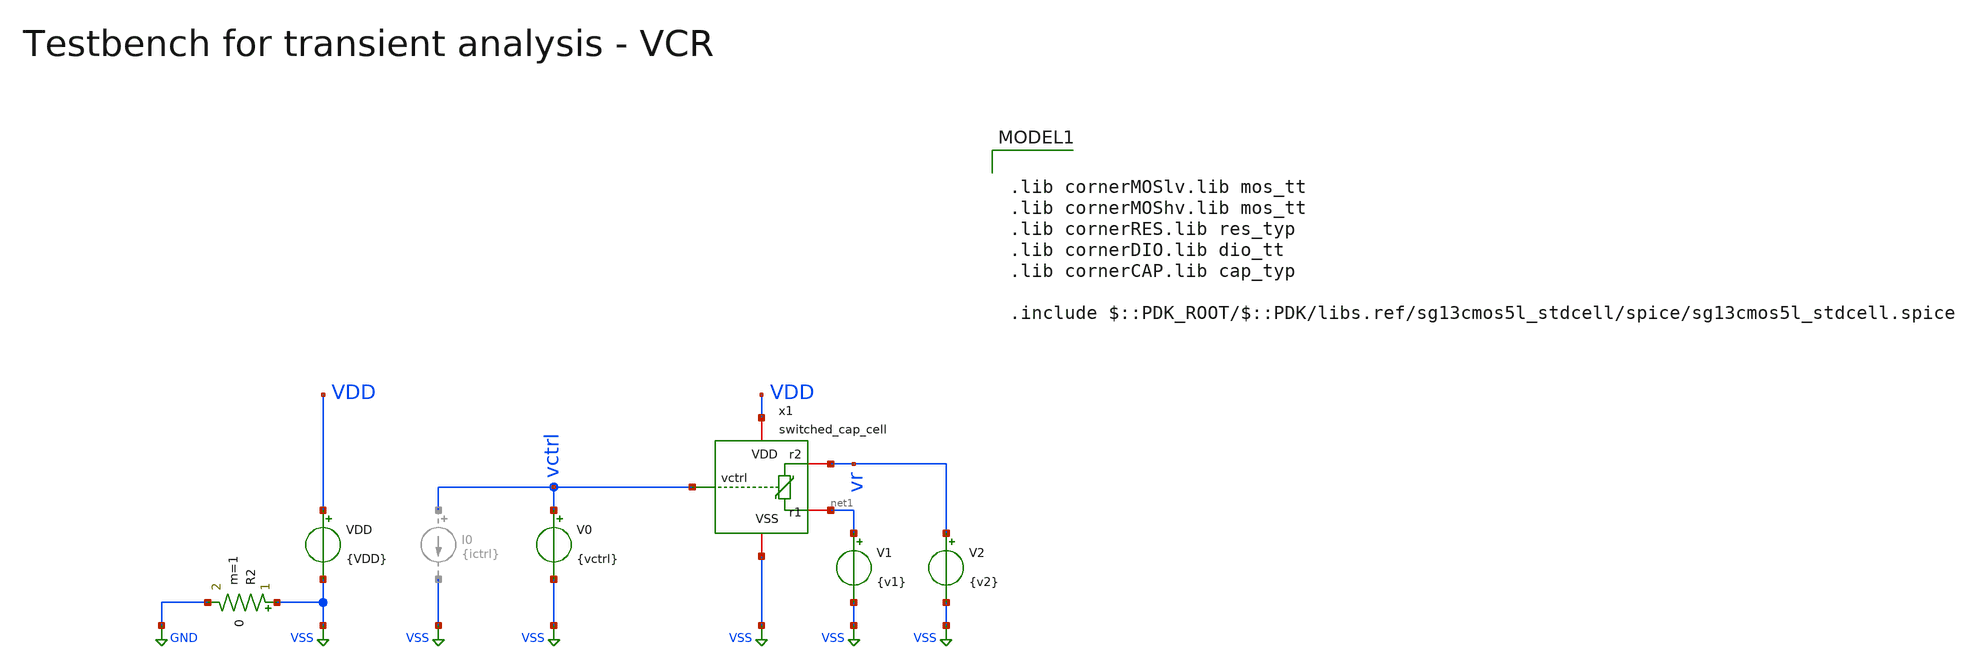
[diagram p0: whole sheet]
** sch_path: macros/heichips26_vcr/macros/switched_capacitor/testbenches/xschem/tb_switched_cap_tran.sch
**.subckt tb_switched_cap_tran
VDD VDD VSS {VDD}
R2 VSS GND 0 m=1
x1 vctrl VDD VSS vr net1 switched_cap_cell
V1 net1 VSS {v1}
V2 vr VSS {v2}
V0 vctrl VSS {vctrl}
**** begin user architecture code

.lib cornerMOSlv.lib mos_tt
.lib cornerMOShv.lib mos_tt
.lib cornerRES.lib res_typ
.lib cornerDIO.lib dio_tt
.lib cornerCAP.lib cap_typ

.include $::PDK_ROOT/$::PDK/libs.ref/sg13cmos5l_stdcell/spice/sg13cmos5l_stdcell.spice



.param temp=27
.param vctrl  = 3.3
.param f      = {2e6/vctrl}

* Derived timing parameters
.param period = {1/f}
.param ton    = {period/2}
.csparam tstop  = {5*period}
.csparam tstep  = {period/100}
.param ictrl  = {f*3.3e-12}
.param tr     = {period/1000}
.param tf     = {period/1000}

.param VDD = 3.3
.csparam VDD=VDD
.param vdm = 3.3
.param vcm = {VDD/2}
.param v1  = {vcm - vdm/2}
.param v2  = {vcm + vdm/2}

.options savecurrents klu method=gear reltol=1e-6 abstol=1e-12 gmin=1e-15
.probe alli
.control

save all
set appendwrite

tran {$&tstep} {$&tstop}
remzerovec

save all
set appendwrite

write @schname\.raw
set appendwrite

*let r_var = vr/i(r1)
meas tran period_sim TRIG i(V1) VAL=1m RISE=1 TARG i(V1) VAL=1m RISE=2
meas tran n_periods TRIG i(V1) VAL=1m RISE=1 TARG i(V1) VAL=1m RISE=LAST
meas tran i_avg AVG i(V1) FROM=0 TO=n_periods
meas tran v_avg AVG vr FROM=0 TO=n_periods
*meas tran r_avg AVG r_var

let npts = length(time) - 1
let i_mavg = integ(i(V1))[1, npts] / time[1, npts]
let v_mavg = integ(vr)[1, npts] / time[1, npts]
let r_mavg = v_mavg/i_mavg
let r_avg = v_avg/i_avg
let f_sim = 1/period_sim
let plot_y_lim = 1.2*r_avg

print period_sim f_sim r_avg

* Plotting
plot vr v_avg v_mavg
plot i(V1) i_avg i_mavg
plot r_avg r_mavg ylimit 0 $&plot_y_lim
plot x1.clk

* Write Data
unset appendwrite
set wr_vecnames
set wr_singlescale
wrdata ../plot_simulations/data/@schname\.txt v(vr) v(VDD) i(V1)

*quit
.endc


**** end user architecture code
**.ends

* expanding   symbol:  switched_cap_cell.sym # of pins=5
** sym_path: macros/heichips26_vcr/macros/switched_capacitor/schematic/xschem/switched_cap_cell.sym
** sch_path: macros/heichips26_vcr/macros/switched_capacitor/schematic/xschem/switched_cap_cell.sch
.subckt switched_cap_cell vctrl VDD VSS r2 r1
*.iopin r1
*.iopin r2
*.iopin VDD
*.iopin VSS
*.iopin vctrl
XC1 net1 VSS cap_cmomi w=30e-6 l=30e-6 mmin=1 mmax=4 feed=double subblock=0 m=1 mm_ok=1
x2 net2 net1 r1 net3 VDD VSS transmission_gate
x6 net5 net1 r2 net4 VDD VSS transmission_gate
x3 net2 net3 VDD clk VSS net5 net4 pulse_shaper
x4 net7 VDD clk VSS VSS VSS VSS net6 net8 hv_mux4
x5 VDD net6 vctrl VSS net9 vco
vselA net7 VSS 0
vselB net8 VSS 3.3
.ends


* expanding   symbol:  transmission_gate.sym # of pins=6
** sym_path: macros/heichips26_vcr/macros/switched_capacitor/schematic/xschem/transmission_gate.sym
** sch_path: macros/heichips26_vcr/macros/switched_capacitor/schematic/xschem/transmission_gate.sch
.subckt transmission_gate vctrl vin vout nvctrl VDD VSS
*.iopin vin
*.iopin vout
*.ipin vctrl
*.ipin nvctrl
*.iopin VDD
*.iopin VSS
XM3 vout vctrl vin VSS sg13_hv_nmos w={tg_ngate_w*tg_ng} l={tg_ch_len} ng={tg_ng} m=1 mm_ok=1
XM4 vout nvctrl vin VDD sg13_hv_pmos w={tg_pgate_w*tg_ng} l={tg_ch_len} ng={tg_ng} m=1 mm_ok=1
**** begin user architecture code


.param tg_ch_len=1u
.param tg_ngate_w=2u
.param tg_pgate_w=10u
.param tg_ng=20


**** end user architecture code
.ends


* expanding   symbol:  osc.sym # of pins=6
** sym_path: macros/heichips26_vcr/macros/switched_capacitor/schematic/xschem/osc.sym
** sch_path: macros/heichips26_vcr/macros/switched_capacitor/schematic/xschem/osc.sch
.subckt osc VDD out1 ictrl VSS start out2
*.iopin VSS
*.iopin VDD
*.iopin out2
*.iopin out1
*.iopin start
*.iopin ictrl
XM3 out1 ictrl VDD VDD sg13_hv_pmos w=10.0u l=2.0u ng=1 m=1 mm_ok=1
XM2 net1 ictrl VDD VDD sg13_hv_pmos w=1u l=2.0u ng=1 m=1 mm_ok=1
XM4 start ictrl VDD VDD sg13_hv_pmos w=1.0u l=2.0u ng=1 m=1 mm_ok=1
XM5 out2 ictrl VDD VDD sg13_hv_pmos w=10.0u l=2.0u ng=1 m=1 mm_ok=1
XM6 ictrl ictrl VDD VDD sg13_hv_pmos w=10.0u l=2.0u ng=1 m=1 mm_ok=1
XC1 net1 out1 cap_cmomi w=10e-6 l=10e-6 mmin=1 mmax=4 feed=double subblock=0 m=1 mm_ok=1
XC2 out2 start cap_cmomi w=10e-6 l=10e-6 mmin=1 mmax=4 feed=double subblock=0 m=1 mm_ok=1
XM8 out1 start VSS VSS sg13_hv_nmos w=3u l=0.45u ng=1 m=1 mm_ok=1
XM1 start start VSS VSS sg13_hv_nmos w=1u l=2u ng=1 m=1 mm_ok=1
XM12 out2 net1 VSS VSS sg13_hv_nmos w=3u l=0.45u ng=1 m=1 mm_ok=1
XM11 net1 net1 VSS VSS sg13_hv_nmos w=1u l=2u ng=1 m=1 mm_ok=1
**** begin user architecture code


.ic v(out1)=0 v(out2)=3.3


**** end user architecture code
.ends


* expanding   symbol:  pulse_shaper.sym # of pins=7
** sym_path: macros/heichips26_vcr/macros/switched_capacitor/schematic/xschem/pulse_shaper.sym
** sch_path: macros/heichips26_vcr/macros/switched_capacitor/schematic/xschem/pulse_shaper.sch
.subckt pulse_shaper out1 nout1 VDD in VSS out2 nout2
*.opin out1
*.opin nout1
*.opin out2
*.opin nout2
*.ipin in
*.iopin VSS
*.iopin VDD
x4 VDD net3 nout2 VSS hv_inverter_40u
x7 VDD net1 net3 VSS low_th_inverter
x8 VDD net1 net2 VSS high_th_inverter
x9 VDD net2 out1 VSS hv_inverter_40u
x10 VDD out1 nout1 VSS hv_inverter_40u
x11 VDD nout2 out2 VSS hv_inverter_40u
**** begin user architecture code


.include ../../../netlist/pex/hv_inverter_0u3_magic_pex_3.spice
.param w   = 0.3u
.param ng  = 1
.param n_ng = ng
.param n_w = {w*n_ng}
.param n_l = 0.45u
.param p_ng = ng
.param p_w = {1*w*p_ng}
.param p_l = 0.4u


**** end user architecture code
x1 VDD in net1 VSS hv_inverter_0u3
.ends


* expanding   symbol:  hv_mux4.sym # of pins=9
** sym_path: macros/heichips26_vcr/macros/switched_capacitor/schematic/xschem/hv_mux4.sym
** sch_path: macros/heichips26_vcr/macros/switched_capacitor/schematic/xschem/hv_mux4.sch
.subckt hv_mux4 selA VDD out VSS in3 in1 in4 in2 selB
*.ipin in1
*.iopin VDD
*.iopin VSS
*.opin out
*.ipin in2
*.ipin selA
*.ipin in3
*.ipin in4
*.ipin selB
x3 VDD selA net9 VSS hv_inverter_40u
x1 VDD net2 out net1 VSS net3 net4 hv_nor4
x2 VDD in1 net2 net6 VSS hv_nor
x4 VDD in2 net1 net7 VSS hv_nor
x5 VDD in3 net3 net8 VSS hv_nor
x6 VDD in4 net4 net5 VSS hv_nor
x7 VDD selA net5 selB VSS hv_nand
x9 VDD net9 net7 selB VSS hv_nand
x10 VDD selB net10 VSS hv_inverter_40u
x11 VDD selA net8 net10 VSS hv_nand
x8 VDD net9 net6 net10 VSS hv_nand
.ends


* expanding   symbol:  vco.sym # of pins=5
** sym_path: macros/heichips26_vcr/macros/switched_capacitor/schematic/xschem/vco.sym
** sch_path: macros/heichips26_vcr/macros/switched_capacitor/schematic/xschem/vco.sch
.subckt vco VDD out vctrl VSS nout
*.iopin VSS
*.iopin VDD
*.iopin nout
*.iopin out
*.iopin vctrl
**** begin user architecture code


.ic v(vc)=1.65


**** end user architecture code
XC1 vc VSS cap_cmomi w=30e-6 l=30e-6 mmin=1 mmax=4 feed=double subblock=0 m=1 mm_ok=1
XM4 vc out 5uA- VSS sg13_hv_nmos w=0.3u l=0.45u ng=1 m=1 mm_ok=1
x1 VDD s out nout r VSS hv_rs-ff
**** begin user architecture code


.param cm_n_w = 6u
.param cm_n_l = 5u
.param cm_p_w = 10u
.param cm_p_l = 2u

.param inv_ng = 1
.param inv_n_w = 2u
.param inv_n_l = 0.45u
.param inv_p_w = 6.5u
.param inv_p_l = 0.4u


**** end user architecture code
XM6 vc out 5uA+ VDD sg13_hv_pmos w=0.3u l=0.4u ng=1 m=1 mm_ok=1
x5 net2 vc vthl VDD 40uA- VSS comp_pmos
x4 VDD net3 VSS current_reference_40uA
XM7 s net1 VSS VSS sg13_hv_nmos w=inv_n_w l=inv_n_l ng=inv_ng m=1 mm_ok=1
XM8 s net1 VDD VDD sg13_hv_pmos w=inv_p_w l=inv_p_l ng=inv_ng m=1 mm_ok=1
XM9 r net2 VSS VSS sg13_hv_nmos w=inv_n_w l=inv_n_l ng=inv_ng m=1 mm_ok=1
XM10 r net2 VDD VDD sg13_hv_pmos w=inv_p_w l=inv_p_l ng=inv_ng m=1 mm_ok=1
x7 net1 vthh vc VDD 40uA+ VSS comp_nmos
XM11 net3 net3 VDD VDD sg13_hv_pmos w=cm_p_w l=cm_p_l ng=1 m=1 mm_ok=1
XM12 40uA+ net3 VDD VDD sg13_hv_pmos w=cm_p_w l=cm_p_l ng=1 m=1 mm_ok=1
XM13 net4 net3 VDD VDD sg13_hv_pmos w=cm_p_w l=cm_p_l ng=1 m=1 mm_ok=1
XM14 net4 net4 VSS VSS sg13_hv_nmos w=cm_n_w l=cm_n_l ng=1 m=1 mm_ok=1
XM15 40uA- net4 VSS VSS sg13_hv_nmos w=cm_n_w l=cm_n_l ng=1 m=1 mm_ok=1
x2 10uA- vthl VDD vctrl VSS vthh voltage_mirror_pmos
XM1 net5 net3 VDD VDD sg13_hv_pmos w=cm_p_w l=cm_p_l ng=1 m=1 mm_ok=1
XM2 net5 net5 VSS VSS sg13_hv_nmos w=4*cm_n_w l=cm_n_l ng=4 m=1 mm_ok=1
XM3 10uA- net5 VSS VSS sg13_hv_nmos w=cm_n_w l=cm_n_l ng=1 m=1 mm_ok=1
XM5 net6 net5 VSS VSS sg13_hv_nmos w=cm_n_w l=cm_n_l ng=1 m=1 mm_ok=1
XM25 net6 net6 VDD VDD sg13_hv_pmos w=2*cm_p_w l=cm_p_l ng=2 m=1 mm_ok=1
XM26 net7 net6 VDD VDD sg13_hv_pmos w=cm_p_w l=cm_p_l ng=1 m=1 mm_ok=1
XM27 5uA+ net6 VDD VDD sg13_hv_pmos w=cm_p_w l=cm_p_l ng=1 m=1 mm_ok=1
XM28 net7 net7 VSS VSS sg13_hv_nmos w=2*cm_n_w l=cm_n_l ng=2 m=1 mm_ok=1
XM29 5uA- net7 VSS VSS sg13_hv_nmos w=cm_n_w l=cm_n_l ng=1 m=1 mm_ok=1
.ends


* expanding   symbol:  hv_inverter_40u.sym # of pins=4
** sym_path: macros/heichips26_vcr/macros/switched_capacitor/schematic/xschem/hv_inverter_40u.sym
** sch_path: macros/heichips26_vcr/macros/switched_capacitor/schematic/xschem/hv_inverter_40u.sch
.subckt hv_inverter_40u VDD in out VSS
*.ipin in
*.iopin VDD
*.iopin VSS
*.opin out
XM2 out in VSS VSS sg13_hv_nmos w={n_w} l={n_l} ng={ng} m=1 mm_ok=1
XM3 out in VDD VDD sg13_hv_pmos w={p_w} l={p_l} ng={ng} m=1 mm_ok=1
**** begin user architecture code


.param w   = 10u
.param ng  = 4
.param n_ng = ng
.param n_w = {3u*n_ng}
.param n_l = 0.45u
.param p_ng = ng
.param p_w = {10u*p_ng}
.param p_l = 0.4u


**** end user architecture code
.ends


* expanding   symbol:  low_th_inverter.sym # of pins=4
** sym_path: macros/heichips26_vcr/macros/switched_capacitor/schematic/xschem/low_th_inverter.sym
** sch_path: macros/heichips26_vcr/macros/switched_capacitor/schematic/xschem/low_th_inverter.sch
.subckt low_th_inverter VDD vin vout VSS
*.ipin vin
*.iopin VDD
*.iopin VSS
*.opin vout
XM1 vout vin VSS VSS sg13_hv_nmos w={n_ng*n_w} l={n_l} ng={n_ng} m=1 mm_ok=1
XM2 vout vin VDD VDD sg13_hv_pmos w={p_ng*p_w} l={p_l} ng={n_ng} m=1 mm_ok=1
**** begin user architecture code


.param n_ng = 2
.param n_w = 1u
.param n_l = 0.45u
.param p_ng = 2
.param p_w = 1u
.param p_l = 0.4u


**** end user architecture code
.ends


* expanding   symbol:  high_th_inverter.sym # of pins=4
** sym_path: macros/heichips26_vcr/macros/switched_capacitor/schematic/xschem/high_th_inverter.sym
** sch_path: macros/heichips26_vcr/macros/switched_capacitor/schematic/xschem/high_th_inverter.sch
.subckt high_th_inverter VDD vin vout VSS
*.ipin vin
*.iopin VDD
*.iopin VSS
*.opin vout
XMdummy1 VSS VSS VSS VSS sg13_hv_nmos w=0.6u l=1.0u ng=2 m=1 mm_ok=1
XMdummy2 VDD VDD VDD VDD sg13_hv_pmos w=12.0u l=1.0u ng=2 m=1 mm_ok=1
XM1 vout vin VSS VSS sg13_hv_nmos w=6.0u l=1.0u ng=20 m=1 mm_ok=1
XM2 vout vin VDD VDD sg13_hv_pmos w=120.0u l=1.0u ng=20 m=1 mm_ok=1
.ends


* expanding   symbol:  hv_inverter_0u3.sym # of pins=4
** sym_path: macros/heichips26_vcr/macros/switched_capacitor/schematic/xschem/hv_inverter_0u3.sym
** sch_path: macros/heichips26_vcr/macros/switched_capacitor/schematic/xschem/hv_inverter_0u3.sch
.subckt hv_inverter_0u3 VDD in out VSS
*.ipin in
*.iopin VDD
*.iopin VSS
*.opin out
XM2 out in VSS VSS sg13_hv_nmos w={n_w} l={n_l} ng={ng} m=1 mm_ok=1
XM3 out in VDD VDD sg13_hv_pmos w={p_w} l={p_l} ng={ng} m=1 mm_ok=1
**** begin user architecture code


.param w   = 0.3u
.param ng  = 1
.param n_ng = ng
.param n_w = {w*n_ng}
.param n_l = 0.45u
.param p_ng = ng
.param p_w = {1*w*p_ng}
.param p_l = 0.4u


**** end user architecture code
.ends


* expanding   symbol:  hv_nor4.sym # of pins=7
** sym_path: macros/heichips26_vcr/macros/switched_capacitor/schematic/xschem/hv_nor4.sym
** sch_path: macros/heichips26_vcr/macros/switched_capacitor/schematic/xschem/hv_nor4.sch
.subckt hv_nor4 VDD in1 out in2 VSS in3 in4
*.ipin in1
*.iopin VDD
*.iopin VSS
*.opin out
*.ipin in2
*.ipin in3
*.ipin in4
**** begin user architecture code


.param w   = 10u
.param ng  = 4
.param n_ng = ng
.param n_w = {3u*n_ng}
.param n_l = 0.45u
.param p_ng = ng
.param p_w = {10u*p_ng}
.param p_l = 0.4u


**** end user architecture code
XM2 out in3 VSS VSS sg13_hv_nmos w={n_w} l={n_l} ng={ng} m=1 mm_ok=1
XM3 net3 in4 VDD VDD sg13_hv_pmos w={p_w} l={p_l} ng={ng} m=1 mm_ok=1
XM1 out in4 VSS VSS sg13_hv_nmos w={n_w} l={n_l} ng={ng} m=1 mm_ok=1
XM4 out in1 net1 VDD sg13_hv_pmos w={p_w} l={p_l} ng={ng} m=1 mm_ok=1
XM5 out in2 VSS VSS sg13_hv_nmos w={n_w} l={n_l} ng={ng} m=1 mm_ok=1
XM6 out in1 VSS VSS sg13_hv_nmos w={n_w} l={n_l} ng={ng} m=1 mm_ok=1
XM7 net1 in2 net2 VDD sg13_hv_pmos w={p_w} l={p_l} ng={ng} m=1 mm_ok=1
XM8 net2 in3 net3 VDD sg13_hv_pmos w={p_w} l={p_l} ng={ng} m=1 mm_ok=1
.ends


* expanding   symbol:  hv_nor.sym # of pins=5
** sym_path: macros/heichips26_vcr/macros/switched_capacitor/schematic/xschem/hv_nor.sym
** sch_path: macros/heichips26_vcr/macros/switched_capacitor/schematic/xschem/hv_nor.sch
.subckt hv_nor VDD in1 out in2 VSS
*.ipin in1
*.iopin VDD
*.iopin VSS
*.opin out
*.ipin in2
**** begin user architecture code


.param w   = 10u
.param ng  = 4
.param n_ng = ng
.param n_w = {3u*n_ng}
.param n_l = 0.45u
.param p_ng = ng
.param p_w = {10u*p_ng}
.param p_l = 0.4u


**** end user architecture code
XM2 out in1 VSS VSS sg13_hv_nmos w={n_w} l={n_l} ng={ng} m=1 mm_ok=1
XM3 net1 in2 VDD VDD sg13_hv_pmos w={p_w} l={p_l} ng={ng} m=1 mm_ok=1
XM1 out in2 VSS VSS sg13_hv_nmos w={n_w} l={n_l} ng={ng} m=1 mm_ok=1
XM4 out in1 net1 VDD sg13_hv_pmos w={p_w} l={p_l} ng={ng} m=1 mm_ok=1
.ends


* expanding   symbol:  hv_nand.sym # of pins=5
** sym_path: macros/heichips26_vcr/macros/switched_capacitor/schematic/xschem/hv_nand.sym
** sch_path: macros/heichips26_vcr/macros/switched_capacitor/schematic/xschem/hv_nand.sch
.subckt hv_nand VDD in1 out in2 VSS
*.ipin in1
*.iopin VDD
*.iopin VSS
*.opin out
*.ipin in2
**** begin user architecture code


.param w   = 10u
.param ng  = 4
.param n_ng = ng
.param n_w = {3u*n_ng}
.param n_l = 0.45u
.param p_ng = ng
.param p_w = {10u*p_ng}
.param p_l = 0.4u


**** end user architecture code
XM2 out in1 net1 VSS sg13_hv_nmos w={n_w} l={n_l} ng={ng} m=1 mm_ok=1
XM3 out in2 VDD VDD sg13_hv_pmos w={p_w} l={p_l} ng={ng} m=1 mm_ok=1
XM1 net1 in2 VSS VSS sg13_hv_nmos w={n_w} l={n_l} ng={ng} m=1 mm_ok=1
XM4 out in1 VDD VDD sg13_hv_pmos w={p_w} l={p_l} ng={ng} m=1 mm_ok=1
.ends


* expanding   symbol:  hv_rs-ff.sym # of pins=6
** sym_path: macros/heichips26_vcr/macros/switched_capacitor/schematic/xschem/hv_rs-ff.sym
** sch_path: macros/heichips26_vcr/macros/switched_capacitor/schematic/xschem/hv_rs-ff.sch
.subckt hv_rs-ff VDD nS Q nQ nR VSS
*.ipin nS
*.iopin VDD
*.iopin VSS
*.opin Q
*.ipin nR
*.opin nQ
x4 VDD nS Q nQ VSS hv_nand
x5 VDD Q nQ nR VSS hv_nand
.ends


* expanding   symbol:  comp_pmos.sym # of pins=6
** sym_path: macros/heichips26_vcr/macros/switched_capacitor/schematic/xschem/comp_pmos.sym
** sch_path: macros/heichips26_vcr/macros/switched_capacitor/schematic/xschem/comp_pmos.sch
.subckt comp_pmos out - + VDD Ibias VSS
*.iopin VDD
*.iopin VSS
*.ipin Ibias
*.opin out
*.ipin +
*.ipin -
**** begin user architecture code


.param n_w = 1.2u
.param n_l = 1.5u
.param p_w = 2u
.param p_l = 0.4u
.param bcm = 1


**** end user architecture code
XM9 net1 Ibias VDD VDD sg13_hv_pmos w=bcm*p_w l=p_l ng=1 m=1 mm_ok=1
XM10 out Ibias VDD VDD sg13_hv_pmos w=bcm*p_w l=p_l ng=1 m=1 mm_ok=1
XM11 Ibias Ibias VDD VDD sg13_hv_pmos w=p_w l=p_l ng=1 m=1 mm_ok=1
XM12 net3 + net1 VDD sg13_hv_pmos w=p_w l=p_l ng=1 m=1 mm_ok=1
XM13 net2 - net1 VDD sg13_hv_pmos w=p_w l=p_l ng=1 m=1 mm_ok=1
XM14 net3 net2 VSS VSS sg13_hv_nmos w=n_w l=n_l ng=1 m=1 mm_ok=1
XM15 net2 net2 VSS VSS sg13_hv_nmos w=n_w l=n_l ng=1 m=1 mm_ok=1
XM16 out net3 VSS VSS sg13_hv_nmos w=n_w l=n_l ng=1 m=1 mm_ok=1
.ends


* expanding   symbol:  current_reference_40uA.sym # of pins=3
** sym_path: macros/heichips26_vcr/macros/switched_capacitor/schematic/xschem/current_reference_40uA.sym
** sch_path: macros/heichips26_vcr/macros/switched_capacitor/schematic/xschem/current_reference_40uA.sch
.subckt current_reference_40uA VDD iout VSS
*.iopin VSS
*.iopin VDD
*.iopin iout
XM8 net2 net2 VSS VSS sg13_hv_nmos w=n_w l=n_l ng=1 m=1 mm_ok=1
XM6 net2 net1 VDD VDD sg13_hv_pmos w=p_w l=p_l ng=1 m=1 mm_ok=1
XM1 net1 net1 VDD VDD sg13_hv_pmos w=p_w l=p_l ng=1 m=1 mm_ok=1
XM3 net1 net2 net3 VSS sg13_hv_nmos w=n_w l=n_l ng=1 m=1 mm_ok=1
XR2 net4 VSS VSS rppd w=2e-6 l=21.9e-6 m=1 b=0 mm_ok=1
XM2 net1 net2 net3 VSS sg13_hv_nmos w=n_w l=n_l ng=1 m=1 mm_ok=1
XM4 net1 net2 net3 VSS sg13_hv_nmos w=n_w l=n_l ng=1 m=1 mm_ok=1
XM5 net1 net2 net3 VSS sg13_hv_nmos w=n_w l=n_l ng=1 m=1 mm_ok=1
XM7 iout net2 VSS VSS sg13_hv_nmos w=n_w l=n_l ng=1 m=1 mm_ok=1
XR3 net3 net4 VSS rsil w=0.5e-6 l=365e-6 m=1 mm_ok=1
**** begin user architecture code


.param n_w = 6u
.param n_l = 5u
.param p_w = 10u
.param p_l = 2u


**** end user architecture code
.ends


* expanding   symbol:  comp_nmos.sym # of pins=6
** sym_path: macros/heichips26_vcr/macros/switched_capacitor/schematic/xschem/comp_nmos.sym
** sch_path: macros/heichips26_vcr/macros/switched_capacitor/schematic/xschem/comp_nmos.sch
.subckt comp_nmos out - + VDD Ibias VSS
*.iopin VDD
*.iopin VSS
*.ipin -
*.ipin +
*.ipin Ibias
*.opin out
XM8 net2 + net3 VSS sg13_hv_nmos w=n_w l=n_l ng=1 m=1 mm_ok=1
XM6 net1 net1 VDD VDD sg13_hv_pmos w=p_w l=p_l ng=1 m=1 mm_ok=1
XM1 net2 net1 VDD VDD sg13_hv_pmos w=p_w l=p_l ng=1 m=1 mm_ok=1
XM3 net1 - net3 VSS sg13_hv_nmos w=n_w l=n_l ng=1 m=1 mm_ok=1
**** begin user architecture code


.param n_w = 1.2u
.param n_l = 1.5u
.param p_w = 2u
.param p_l = 0.4u


**** end user architecture code
XM2 out net2 VDD VDD sg13_hv_pmos w=p_w l=p_l ng=1 m=1 mm_ok=1
XM4 net3 Ibias VSS VSS sg13_hv_nmos w=2*n_w l=n_l ng=1 m=1 mm_ok=1
XM5 out Ibias VSS VSS sg13_hv_nmos w=2*n_w l=n_l ng=1 m=1 mm_ok=1
XM7 Ibias Ibias VSS VSS sg13_hv_nmos w=n_w l=n_l ng=1 m=1 mm_ok=1
.ends


* expanding   symbol:  voltage_mirror_pmos.sym # of pins=6
** sym_path: macros/heichips26_vcr/macros/switched_capacitor/schematic/xschem/voltage_mirror_pmos.sym
** sch_path: macros/heichips26_vcr/macros/switched_capacitor/schematic/xschem/voltage_mirror_pmos.sch
.subckt voltage_mirror_pmos Ibias nout VDD in VSS out
*.iopin VDD
*.iopin VSS
*.ipin in
*.opin out
*.opin nout
*.ipin Ibias
**** begin user architecture code


.param n_w = 6u
.param n_l = 5u
.param p_w = 10u
.param p_l = 2u


**** end user architecture code
XR1 in Ibias VSS rhigh w=0.5e-6 l=34e-6 m=1 b=0 mm_ok=1
XM4 net1 Ibias VDD VDD sg13_hv_pmos w=p_w l=p_l ng=1 m=1 mm_ok=1
XM5 out net1 VSS VSS sg13_hv_nmos w=n_w l=n_l ng=1 m=1 mm_ok=1
XR2 VSS nout VSS rhigh w=0.5e-6 l=34e-6 m=1 b=0 mm_ok=1
XR3 out VDD VSS rhigh w=0.5e-6 l=34e-6 m=1 b=0 mm_ok=1
XM2 net1 net1 VSS VSS sg13_hv_nmos w=n_w l=n_l ng=1 m=1 mm_ok=1
XM3 nout Ibias VDD VDD sg13_hv_pmos w=p_w l=p_l ng=1 m=1 mm_ok=1
XM6 Ibias Ibias VDD VDD sg13_hv_pmos w=1.9*p_w l=p_l ng=1 m=1 mm_ok=1
.ends

.GLOBAL VSS
.GLOBAL GND
.end
